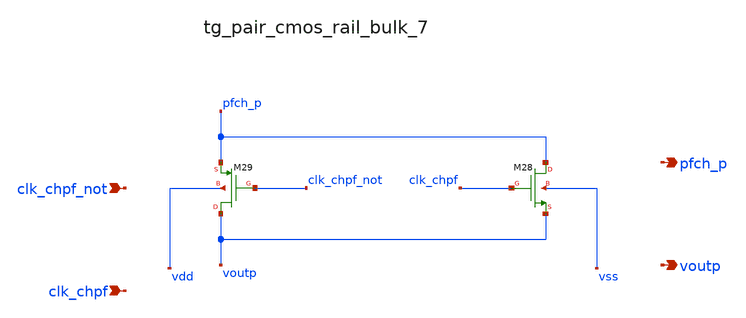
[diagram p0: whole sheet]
** sch_path: analog-db/raw/ia_003_fan_chopper_pf/hier/blocks/tg_pair_cmos_rail_bulk_7.sch
**.subckt tg_pair_cmos_rail_bulk_7 clk_chpf_not clk_chpf pfch_p voutp
*.ipin clk_chpf_not
*.ipin clk_chpf
*.opin pfch_p
*.opin voutp
XM28 pfch_p clk_chpf voutp vss sg13_lv_nmos w=x_dut_xm28_w l=x_dut_xm28_l ng=1 m=x_dut_xm28_m
XM29 voutp clk_chpf_not pfch_p vdd sg13_lv_pmos w=x_dut_xm29_w l=x_dut_xm29_l ng=1 m=x_dut_xm29_m
**.ends
.end
